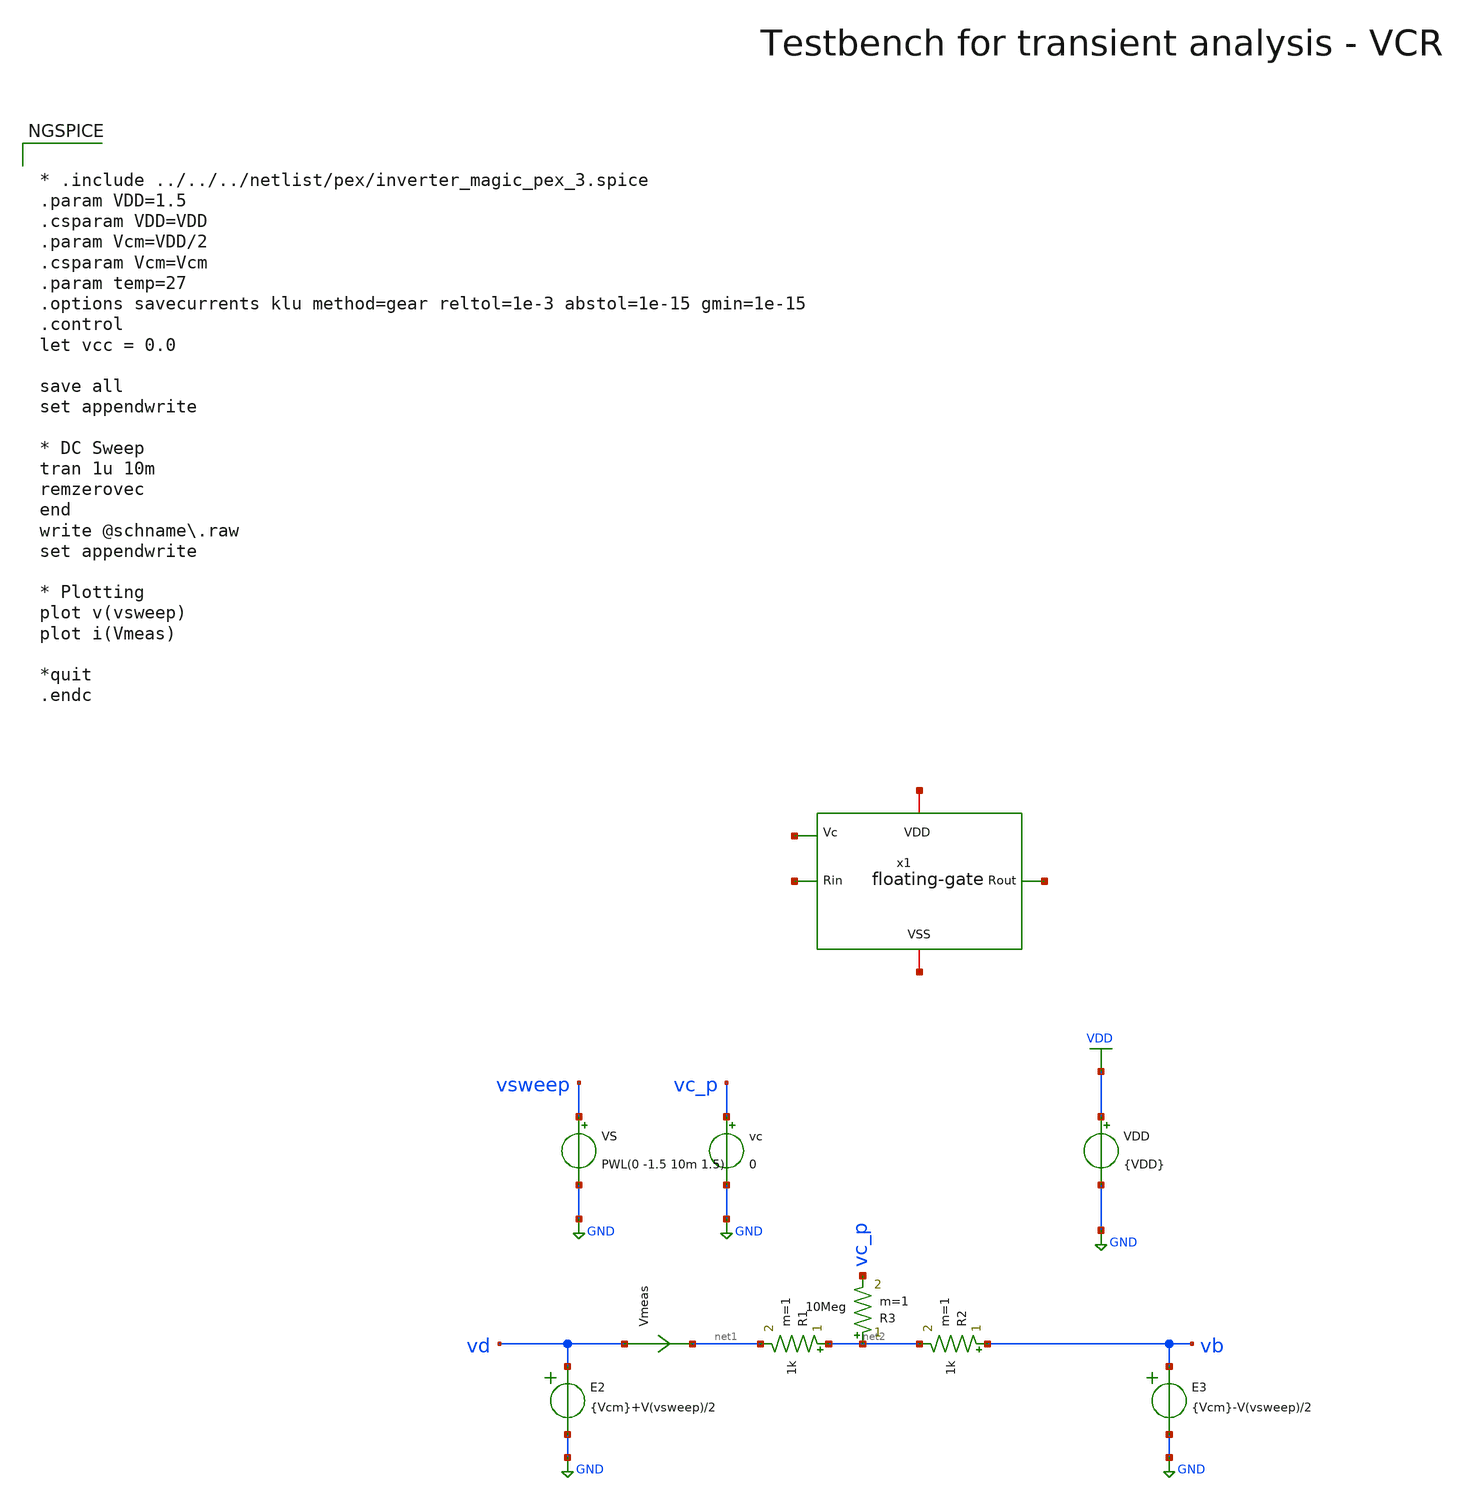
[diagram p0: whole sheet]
** sch_path: macros/heichips26_analog_project/macros/floating-gate/testbenches/xschem/res_tb_tran2.sch
**.subckt res_tb_tran2
VDD VDD GND {VDD}
R1 net2 net1 1k m=1
VS vsweep GND PWL(0 -1.5 10m 1.5)
Vmeas vd net1 0
.save i(vmeas)
E2 vd GND VOL=' {Vcm}+V(vsweep)/2 '
E3 vb GND VOL=' {Vcm}-V(vsweep)/2 '
vc vc_p GND 0
R2 vb net2 1k m=1
R3 net2 vc_p 10Meg m=1
x1 net3 net4 net5 net6 net7 floating-gate
**** begin user architecture code

.lib cornerMOSlv.lib mos_tt
.lib cornerMOShv.lib mos_tt
.lib cornerRES.lib res_typ
.lib cornerDIO.lib dio_tt



* .include ../../../netlist/pex/inverter_magic_pex_3.spice
.param VDD=1.5
.csparam VDD=VDD
.param Vcm=VDD/2
.csparam Vcm=Vcm
.param temp=27
.options savecurrents klu method=gear reltol=1e-3 abstol=1e-15 gmin=1e-15
.control
let vcc = 0.0

save all
set appendwrite

* DC Sweep
tran 1u 10m
remzerovec
end
write @schname\.raw
set appendwrite

* Plotting
plot v(vsweep)
plot i(Vmeas)

*quit
.endc


**** end user architecture code
**.ends

* expanding   symbol:
*+  /home/raiku/k/heichips26-voltage-controlled-resistor/macros/heichips26_analog_project/macros/floating-gate/schematic/xschem/floating-gate.sym # of pins=5
** sym_path: macros/heichips26_analog_project/macros/floating-gate/schematic/xschem/floating-gate.sym
** sch_path: macros/heichips26_analog_project/macros/floating-gate/schematic/xschem/floating-gate.sch
.subckt floating-gate Rin VDD VSS Rout Vc
*.opin Rout
*.ipin Vc
*.ipin Rin
*.iopin VSS
*.opin Rout
*.ipin Vc
*.ipin Rin
*.iopin VSS
*.ipin VDD
*.iopin VSS
*.iopin VSS
XM5 net2 net3 net1 net4 sg13_hv_nmos w=7u l=4u ng=20 m=1 mm_ok=1
XM1 net2 net2 net1 net4 sg13_hv_nmos w=7u l=4u ng=20 m=1 mm_ok=1
XM2 Rin Rin net5 VSS sg13_hv_nmos w=7u l=4u ng=20 m=1 mm_ok=1
XM3 VDD VDD net5 VSS sg13_hv_nmos w=7u l=4u ng=20 m=1 mm_ok=1
XM4 Rin Vc Rout VSS sg13_hv_nmos w=7u l=4u ng=20 m=1 mm_ok=1
XM6 net5 Vc Rout VSS sg13_hv_nmos w=7u l=4u ng=20 m=1 mm_ok=1
.ends

.GLOBAL GND
.GLOBAL VDD
.end
